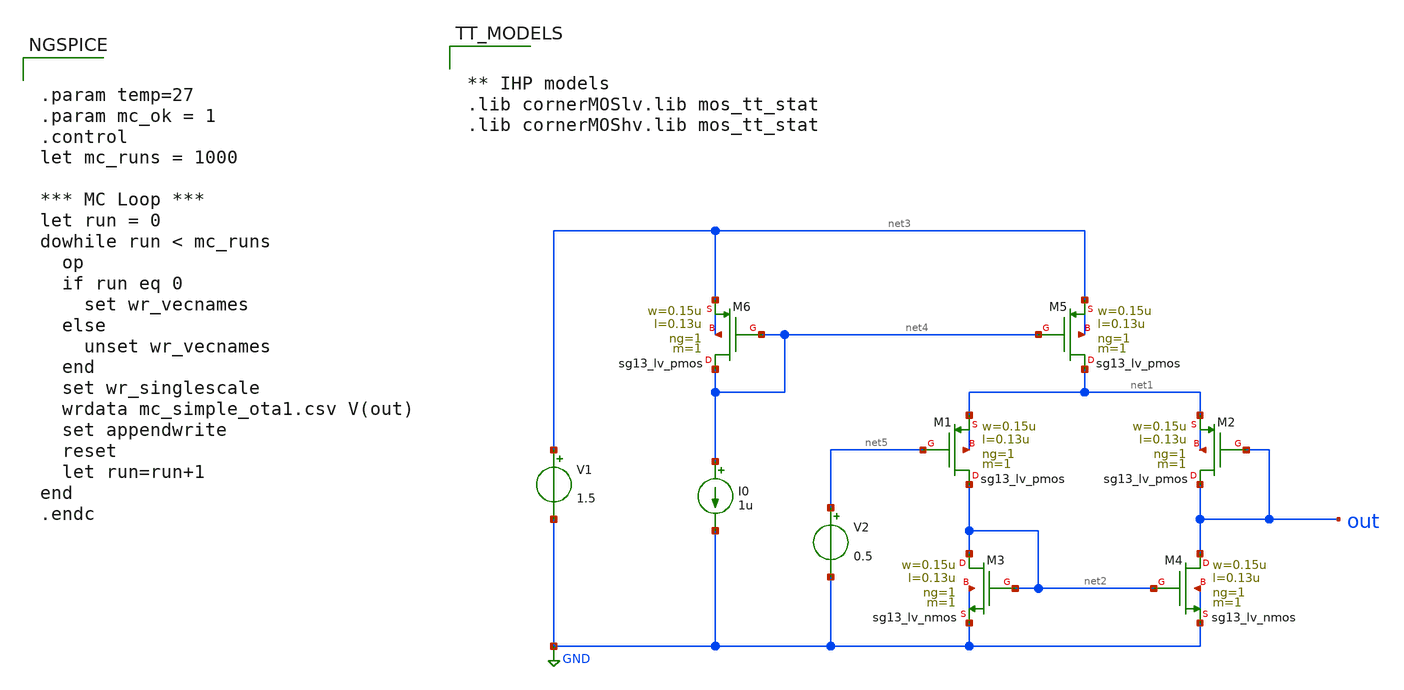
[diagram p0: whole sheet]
** sch_path: 10_xschem/mc_simple_ota1.sch
**.subckt mc_simple_ota1
V1 net3 GND 1.5
XM1 net2 net5 net1 net1 sg13_lv_pmos w=0.15u l=0.13u ng=1 m=1 mm_ok=1
XM2 out out net1 net1 sg13_lv_pmos w=0.15u l=0.13u ng=1 m=1 mm_ok=1
XM3 net2 net2 GND GND sg13_lv_nmos w=0.15u l=0.13u ng=1 m=1 mm_ok=1
XM4 out net2 GND GND sg13_lv_nmos w=0.15u l=0.13u ng=1 m=1 mm_ok=1
XM5 net1 net4 net3 net3 sg13_lv_pmos w=0.15u l=0.13u ng=1 m=1 mm_ok=1
XM6 net4 net4 net3 net3 sg13_lv_pmos w=0.15u l=0.13u ng=1 m=1 mm_ok=1
I0 net4 GND 1u
V2 net5 GND 0.5
**** begin user architecture code


.param temp=27
.param mc_ok = 1
.control
let mc_runs = 1000

*** MC Loop ***
let run = 0
dowhile run < mc_runs
  op
  if run eq 0
    set wr_vecnames
  else
    unset wr_vecnames
  end
  set wr_singlescale
  wrdata mc_simple_ota1.csv V(out)
  set appendwrite
  reset
  let run=run+1
end
.endc




** IHP models
.lib cornerMOSlv.lib mos_tt_stat
.lib cornerMOShv.lib mos_tt_stat


**** end user architecture code
**.ends
.GLOBAL GND
.end
